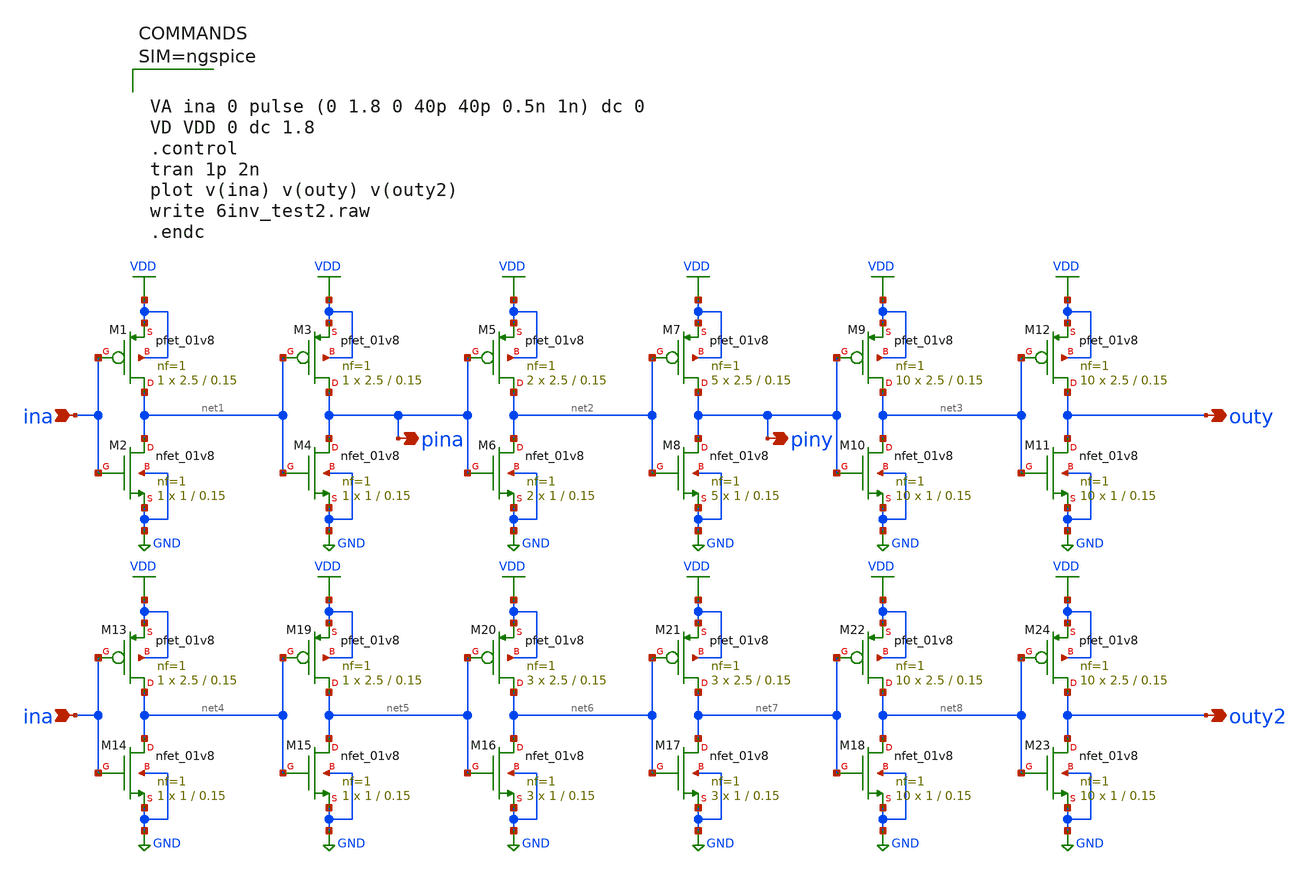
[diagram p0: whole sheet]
** sch_path: 6inv_test2.sch
**.subckt 6inv_test2 ina outy pina piny ina outy2
*.ipin ina
*.opin outy
*.opin pina
*.opin piny
*.ipin ina
*.opin outy2
XM1 net1 ina VDD VDD sky130_fd_pr__pfet_01v8 L=0.15 W=2.5 nf=1 ad='int((nf+1)/2) * W/nf * 0.29' as='int((nf+2)/2) * W/nf * 0.29'
+ pd='2*int((nf+1)/2) * (W/nf + 0.29)' ps='2*int((nf+2)/2) * (W/nf + 0.29)' nrd='0.29 / W' nrs='0.29 / W'
+ sa=0 sb=0 sd=0 mult=1 m=1
XM2 net1 ina GND GND sky130_fd_pr__nfet_01v8 L=0.15 W=1 nf=1 ad='int((nf+1)/2) * W/nf * 0.29' as='int((nf+2)/2) * W/nf * 0.29'
+ pd='2*int((nf+1)/2) * (W/nf + 0.29)' ps='2*int((nf+2)/2) * (W/nf + 0.29)' nrd='0.29 / W' nrs='0.29 / W'
+ sa=0 sb=0 sd=0 mult=1 m=1
XM4 pina net1 GND GND sky130_fd_pr__nfet_01v8 L=0.15 W=1 nf=1 ad='int((nf+1)/2) * W/nf * 0.29' as='int((nf+2)/2) * W/nf * 0.29'
+ pd='2*int((nf+1)/2) * (W/nf + 0.29)' ps='2*int((nf+2)/2) * (W/nf + 0.29)' nrd='0.29 / W' nrs='0.29 / W'
+ sa=0 sb=0 sd=0 mult=1 m=1
XM6 net2 pina GND GND sky130_fd_pr__nfet_01v8 L=0.15 W=1 nf=1 ad='int((nf+1)/2) * W/nf * 0.29' as='int((nf+2)/2) * W/nf * 0.29'
+ pd='2*int((nf+1)/2) * (W/nf + 0.29)' ps='2*int((nf+2)/2) * (W/nf + 0.29)' nrd='0.29 / W' nrs='0.29 / W'
+ sa=0 sb=0 sd=0 mult=2 m=2
XM8 piny net2 GND GND sky130_fd_pr__nfet_01v8 L=0.15 W=1 nf=1 ad='int((nf+1)/2) * W/nf * 0.29' as='int((nf+2)/2) * W/nf * 0.29'
+ pd='2*int((nf+1)/2) * (W/nf + 0.29)' ps='2*int((nf+2)/2) * (W/nf + 0.29)' nrd='0.29 / W' nrs='0.29 / W'
+ sa=0 sb=0 sd=0 mult=5 m=5
XM10 net3 piny GND GND sky130_fd_pr__nfet_01v8 L=0.15 W=1 nf=1 ad='int((nf+1)/2) * W/nf * 0.29' as='int((nf+2)/2) * W/nf * 0.29'
+ pd='2*int((nf+1)/2) * (W/nf + 0.29)' ps='2*int((nf+2)/2) * (W/nf + 0.29)' nrd='0.29 / W' nrs='0.29 / W'
+ sa=0 sb=0 sd=0 mult=10 m=10
XM3 pina net1 VDD VDD sky130_fd_pr__pfet_01v8 L=0.15 W=2.5 nf=1 ad='int((nf+1)/2) * W/nf * 0.29' as='int((nf+2)/2) * W/nf * 0.29'
+ pd='2*int((nf+1)/2) * (W/nf + 0.29)' ps='2*int((nf+2)/2) * (W/nf + 0.29)' nrd='0.29 / W' nrs='0.29 / W'
+ sa=0 sb=0 sd=0 mult=1 m=1
XM5 net2 pina VDD VDD sky130_fd_pr__pfet_01v8 L=0.15 W=2.5 nf=1 ad='int((nf+1)/2) * W/nf * 0.29' as='int((nf+2)/2) * W/nf * 0.29'
+ pd='2*int((nf+1)/2) * (W/nf + 0.29)' ps='2*int((nf+2)/2) * (W/nf + 0.29)' nrd='0.29 / W' nrs='0.29 / W'
+ sa=0 sb=0 sd=0 mult=2 m=2
XM7 piny net2 VDD VDD sky130_fd_pr__pfet_01v8 L=0.15 W=2.5 nf=1 ad='int((nf+1)/2) * W/nf * 0.29' as='int((nf+2)/2) * W/nf * 0.29'
+ pd='2*int((nf+1)/2) * (W/nf + 0.29)' ps='2*int((nf+2)/2) * (W/nf + 0.29)' nrd='0.29 / W' nrs='0.29 / W'
+ sa=0 sb=0 sd=0 mult=5 m=5
XM9 net3 piny VDD VDD sky130_fd_pr__pfet_01v8 L=0.15 W=2.5 nf=1 ad='int((nf+1)/2) * W/nf * 0.29' as='int((nf+2)/2) * W/nf * 0.29'
+ pd='2*int((nf+1)/2) * (W/nf + 0.29)' ps='2*int((nf+2)/2) * (W/nf + 0.29)' nrd='0.29 / W' nrs='0.29 / W'
+ sa=0 sb=0 sd=0 mult=10 m=10
XM11 outy net3 GND GND sky130_fd_pr__nfet_01v8 L=0.15 W=1 nf=1 ad='int((nf+1)/2) * W/nf * 0.29' as='int((nf+2)/2) * W/nf * 0.29'
+ pd='2*int((nf+1)/2) * (W/nf + 0.29)' ps='2*int((nf+2)/2) * (W/nf + 0.29)' nrd='0.29 / W' nrs='0.29 / W'
+ sa=0 sb=0 sd=0 mult=10 m=10
XM12 outy net3 VDD VDD sky130_fd_pr__pfet_01v8 L=0.15 W=2.5 nf=1 ad='int((nf+1)/2) * W/nf * 0.29' as='int((nf+2)/2) * W/nf * 0.29'
+ pd='2*int((nf+1)/2) * (W/nf + 0.29)' ps='2*int((nf+2)/2) * (W/nf + 0.29)' nrd='0.29 / W' nrs='0.29 / W'
+ sa=0 sb=0 sd=0 mult=10 m=10
XM13 net4 ina VDD VDD sky130_fd_pr__pfet_01v8 L=0.15 W=2.5 nf=1 ad='int((nf+1)/2) * W/nf * 0.29' as='int((nf+2)/2) * W/nf * 0.29'
+ pd='2*int((nf+1)/2) * (W/nf + 0.29)' ps='2*int((nf+2)/2) * (W/nf + 0.29)' nrd='0.29 / W' nrs='0.29 / W'
+ sa=0 sb=0 sd=0 mult=1 m=1
XM14 net4 ina GND GND sky130_fd_pr__nfet_01v8 L=0.15 W=1 nf=1 ad='int((nf+1)/2) * W/nf * 0.29' as='int((nf+2)/2) * W/nf * 0.29'
+ pd='2*int((nf+1)/2) * (W/nf + 0.29)' ps='2*int((nf+2)/2) * (W/nf + 0.29)' nrd='0.29 / W' nrs='0.29 / W'
+ sa=0 sb=0 sd=0 mult=1 m=1
XM15 net5 net4 GND GND sky130_fd_pr__nfet_01v8 L=0.15 W=1 nf=1 ad='int((nf+1)/2) * W/nf * 0.29' as='int((nf+2)/2) * W/nf * 0.29'
+ pd='2*int((nf+1)/2) * (W/nf + 0.29)' ps='2*int((nf+2)/2) * (W/nf + 0.29)' nrd='0.29 / W' nrs='0.29 / W'
+ sa=0 sb=0 sd=0 mult=1 m=1
XM16 net6 net5 GND GND sky130_fd_pr__nfet_01v8 L=0.15 W=1 nf=1 ad='int((nf+1)/2) * W/nf * 0.29' as='int((nf+2)/2) * W/nf * 0.29'
+ pd='2*int((nf+1)/2) * (W/nf + 0.29)' ps='2*int((nf+2)/2) * (W/nf + 0.29)' nrd='0.29 / W' nrs='0.29 / W'
+ sa=0 sb=0 sd=0 mult=3 m=3
XM17 net7 net6 GND GND sky130_fd_pr__nfet_01v8 L=0.15 W=1 nf=1 ad='int((nf+1)/2) * W/nf * 0.29' as='int((nf+2)/2) * W/nf * 0.29'
+ pd='2*int((nf+1)/2) * (W/nf + 0.29)' ps='2*int((nf+2)/2) * (W/nf + 0.29)' nrd='0.29 / W' nrs='0.29 / W'
+ sa=0 sb=0 sd=0 mult=3 m=3
XM18 net8 net7 GND GND sky130_fd_pr__nfet_01v8 L=0.15 W=1 nf=1 ad='int((nf+1)/2) * W/nf * 0.29' as='int((nf+2)/2) * W/nf * 0.29'
+ pd='2*int((nf+1)/2) * (W/nf + 0.29)' ps='2*int((nf+2)/2) * (W/nf + 0.29)' nrd='0.29 / W' nrs='0.29 / W'
+ sa=0 sb=0 sd=0 mult=10 m=10
XM19 net5 net4 VDD VDD sky130_fd_pr__pfet_01v8 L=0.15 W=2.5 nf=1 ad='int((nf+1)/2) * W/nf * 0.29' as='int((nf+2)/2) * W/nf * 0.29'
+ pd='2*int((nf+1)/2) * (W/nf + 0.29)' ps='2*int((nf+2)/2) * (W/nf + 0.29)' nrd='0.29 / W' nrs='0.29 / W'
+ sa=0 sb=0 sd=0 mult=1 m=1
XM20 net6 net5 VDD VDD sky130_fd_pr__pfet_01v8 L=0.15 W=2.5 nf=1 ad='int((nf+1)/2) * W/nf * 0.29' as='int((nf+2)/2) * W/nf * 0.29'
+ pd='2*int((nf+1)/2) * (W/nf + 0.29)' ps='2*int((nf+2)/2) * (W/nf + 0.29)' nrd='0.29 / W' nrs='0.29 / W'
+ sa=0 sb=0 sd=0 mult=3 m=3
XM21 net7 net6 VDD VDD sky130_fd_pr__pfet_01v8 L=0.15 W=2.5 nf=1 ad='int((nf+1)/2) * W/nf * 0.29' as='int((nf+2)/2) * W/nf * 0.29'
+ pd='2*int((nf+1)/2) * (W/nf + 0.29)' ps='2*int((nf+2)/2) * (W/nf + 0.29)' nrd='0.29 / W' nrs='0.29 / W'
+ sa=0 sb=0 sd=0 mult=3 m=3
XM22 net8 net7 VDD VDD sky130_fd_pr__pfet_01v8 L=0.15 W=2.5 nf=1 ad='int((nf+1)/2) * W/nf * 0.29' as='int((nf+2)/2) * W/nf * 0.29'
+ pd='2*int((nf+1)/2) * (W/nf + 0.29)' ps='2*int((nf+2)/2) * (W/nf + 0.29)' nrd='0.29 / W' nrs='0.29 / W'
+ sa=0 sb=0 sd=0 mult=10 m=10
XM23 outy2 net8 GND GND sky130_fd_pr__nfet_01v8 L=0.15 W=1 nf=1 ad='int((nf+1)/2) * W/nf * 0.29' as='int((nf+2)/2) * W/nf * 0.29'
+ pd='2*int((nf+1)/2) * (W/nf + 0.29)' ps='2*int((nf+2)/2) * (W/nf + 0.29)' nrd='0.29 / W' nrs='0.29 / W'
+ sa=0 sb=0 sd=0 mult=10 m=10
XM24 outy2 net8 VDD VDD sky130_fd_pr__pfet_01v8 L=0.15 W=2.5 nf=1 ad='int((nf+1)/2) * W/nf * 0.29' as='int((nf+2)/2) * W/nf * 0.29'
+ pd='2*int((nf+1)/2) * (W/nf + 0.29)' ps='2*int((nf+2)/2) * (W/nf + 0.29)' nrd='0.29 / W' nrs='0.29 / W'
+ sa=0 sb=0 sd=0 mult=10 m=10
**** begin user architecture code

** opencircuitdesign pdks install
.lib $::SKYWATER_MODELS/sky130.lib.spice ss





VA ina 0 pulse (0 1.8 0 40p 40p 0.5n 1n) dc 0
VD VDD 0 dc 1.8
.control
tran 1p 2n
plot v(ina) v(outy) v(outy2)
write 6inv_test2.raw
.endc



**** end user architecture code
**.ends
.GLOBAL GND
.GLOBAL VDD
.end
